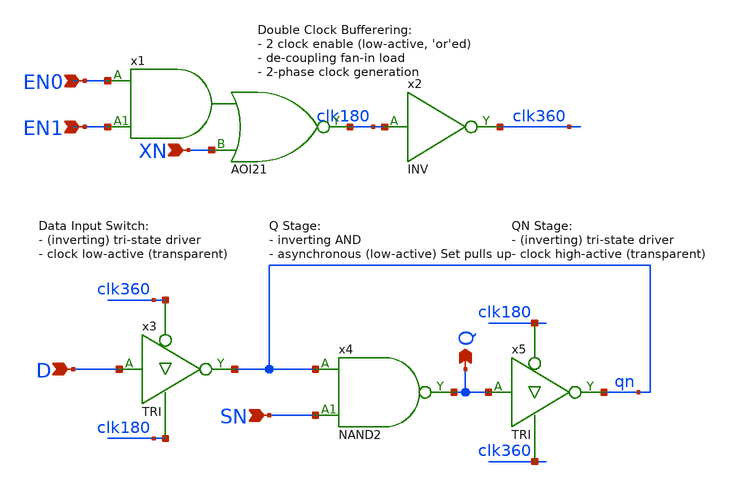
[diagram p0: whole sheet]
** sch_path: Sources/crafted/LATNEES.sch
**.subckt LATNEES XN D Q EN0 EN1 SN
*.ipin XN
*.ipin D
*.opin Q
*.ipin EN0
*.ipin EN1
*.ipin SN
x1 EN0 EN1 XN clk180 VDD GND AOI21 Wmin=1.5u Lmin=1u g=2 m=1
x2 clk180 clk360 VDD GND INV Wmin=1.5u Lmin=1u g=2 m=1
x3 D clk360 clk180 qn VDD GND TRI Wmin=1.5u Lmin=1u g=2 m=1
x5 Q clk180 clk360 qn VDD GND TRI Wmin=1.5u Lmin=1u g=2 m=1
x4 qn SN Q VDD GND NAND2 Wmin=1.5u Lmin=1u g=2 m=1
**.ends
.end
